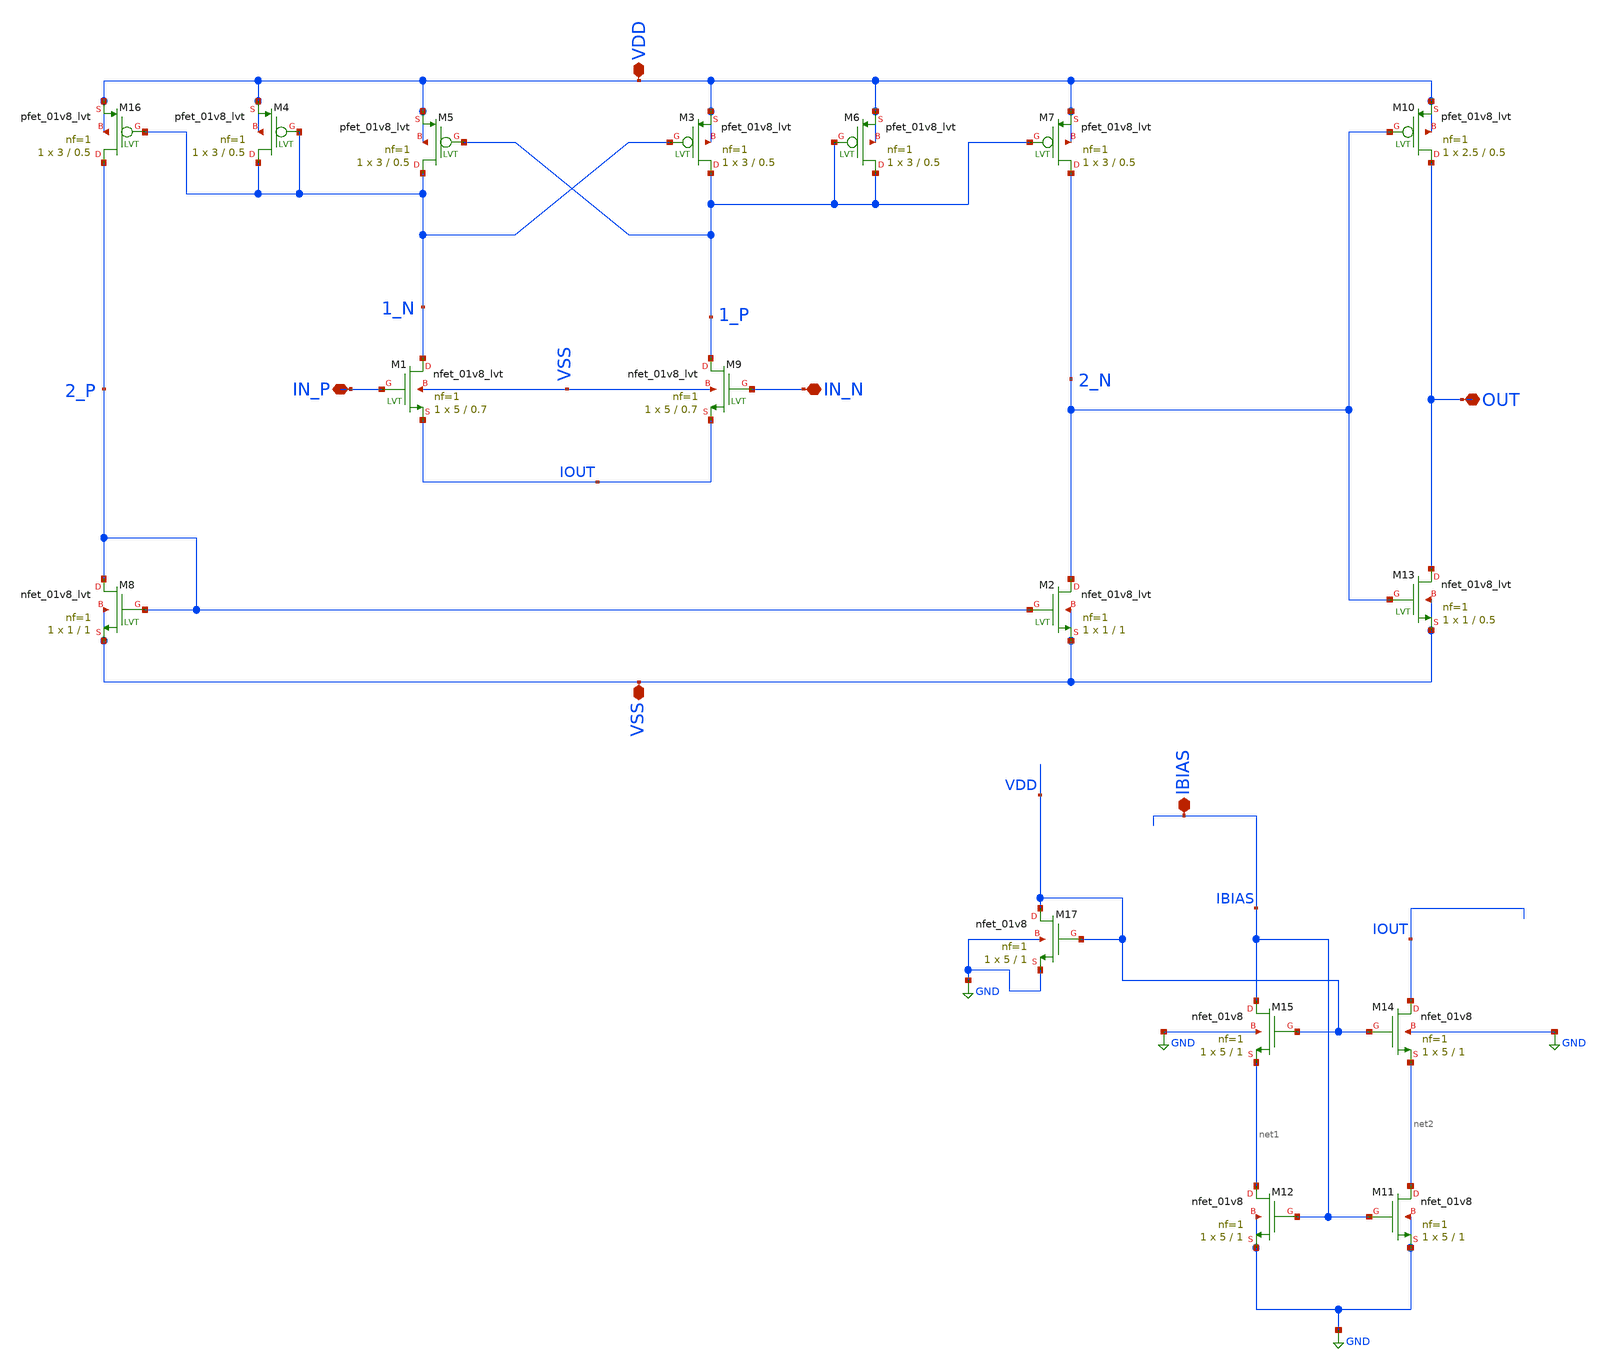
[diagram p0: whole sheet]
** sch_path: xschem/DC_DC_Converter_xschem/OTHERS/DC_DC_Converter_JV11/Comparator/comp_lvt_current_mirror.sch
**.subckt comp_lvt_current_mirror VSS VDD IN_P IN_N OUT IBIAS
*.iopin VSS
*.iopin VDD
*.iopin IN_P
*.iopin IN_N
*.iopin OUT
*.iopin IBIAS
XM16 2_P 1_N VDD VDD sky130_fd_pr__pfet_01v8_lvt L=0.5 W=3 nf=1 ad='int((nf+1)/2) * W/nf * 0.29' as='int((nf+2)/2) * W/nf * 0.29'
+ pd='2*int((nf+1)/2) * (W/nf + 0.29)' ps='2*int((nf+2)/2) * (W/nf + 0.29)' nrd='0.29 / W' nrs='0.29 / W'
+ sa=0 sb=0 sd=0 mult=1 m=1
XM4 1_N 1_N VDD VDD sky130_fd_pr__pfet_01v8_lvt L=0.5 W=3 nf=1 ad='int((nf+1)/2) * W/nf * 0.29' as='int((nf+2)/2) * W/nf * 0.29'
+ pd='2*int((nf+1)/2) * (W/nf + 0.29)' ps='2*int((nf+2)/2) * (W/nf + 0.29)' nrd='0.29 / W' nrs='0.29 / W'
+ sa=0 sb=0 sd=0 mult=1 m=1
XM5 1_N 1_P VDD VDD sky130_fd_pr__pfet_01v8_lvt L=0.5 W=3 nf=1 ad='int((nf+1)/2) * W/nf * 0.29' as='int((nf+2)/2) * W/nf * 0.29'
+ pd='2*int((nf+1)/2) * (W/nf + 0.29)' ps='2*int((nf+2)/2) * (W/nf + 0.29)' nrd='0.29 / W' nrs='0.29 / W'
+ sa=0 sb=0 sd=0 mult=1 m=1
XM3 1_P 1_N VDD VDD sky130_fd_pr__pfet_01v8_lvt L=0.5 W=3 nf=1 ad='int((nf+1)/2) * W/nf * 0.29' as='int((nf+2)/2) * W/nf * 0.29'
+ pd='2*int((nf+1)/2) * (W/nf + 0.29)' ps='2*int((nf+2)/2) * (W/nf + 0.29)' nrd='0.29 / W' nrs='0.29 / W'
+ sa=0 sb=0 sd=0 mult=1 m=1
XM6 1_P 1_P VDD VDD sky130_fd_pr__pfet_01v8_lvt L=0.5 W=3 nf=1 ad='int((nf+1)/2) * W/nf * 0.29' as='int((nf+2)/2) * W/nf * 0.29'
+ pd='2*int((nf+1)/2) * (W/nf + 0.29)' ps='2*int((nf+2)/2) * (W/nf + 0.29)' nrd='0.29 / W' nrs='0.29 / W'
+ sa=0 sb=0 sd=0 mult=1 m=1
XM7 2_N 1_P VDD VDD sky130_fd_pr__pfet_01v8_lvt L=0.5 W=3 nf=1 ad='int((nf+1)/2) * W/nf * 0.29' as='int((nf+2)/2) * W/nf * 0.29'
+ pd='2*int((nf+1)/2) * (W/nf + 0.29)' ps='2*int((nf+2)/2) * (W/nf + 0.29)' nrd='0.29 / W' nrs='0.29 / W'
+ sa=0 sb=0 sd=0 mult=1 m=1
XM8 2_P 2_P VSS VSS sky130_fd_pr__nfet_01v8_lvt L=1 W=1 nf=1 ad='int((nf+1)/2) * W/nf * 0.29' as='int((nf+2)/2) * W/nf * 0.29'
+ pd='2*int((nf+1)/2) * (W/nf + 0.29)' ps='2*int((nf+2)/2) * (W/nf + 0.29)' nrd='0.29 / W' nrs='0.29 / W'
+ sa=0 sb=0 sd=0 mult=1 m=1
XM2 2_N 2_P VSS VSS sky130_fd_pr__nfet_01v8_lvt L=1 W=1 nf=1 ad='int((nf+1)/2) * W/nf * 0.29' as='int((nf+2)/2) * W/nf * 0.29'
+ pd='2*int((nf+1)/2) * (W/nf + 0.29)' ps='2*int((nf+2)/2) * (W/nf + 0.29)' nrd='0.29 / W' nrs='0.29 / W'
+ sa=0 sb=0 sd=0 mult=1 m=1
XM9 1_P IN_N IOUT VSS sky130_fd_pr__nfet_01v8_lvt L=0.7 W=5 nf=1 ad='int((nf+1)/2) * W/nf * 0.29' as='int((nf+2)/2) * W/nf * 0.29'
+ pd='2*int((nf+1)/2) * (W/nf + 0.29)' ps='2*int((nf+2)/2) * (W/nf + 0.29)' nrd='0.29 / W' nrs='0.29 / W'
+ sa=0 sb=0 sd=0 mult=1 m=1
XM1 1_N IN_P IOUT VSS sky130_fd_pr__nfet_01v8_lvt L=0.7 W=5 nf=1 ad='int((nf+1)/2) * W/nf * 0.29' as='int((nf+2)/2) * W/nf * 0.29'
+ pd='2*int((nf+1)/2) * (W/nf + 0.29)' ps='2*int((nf+2)/2) * (W/nf + 0.29)' nrd='0.29 / W' nrs='0.29 / W'
+ sa=0 sb=0 sd=0 mult=1 m=1
XM10 OUT 2_N VDD VDD sky130_fd_pr__pfet_01v8_lvt L=0.5 W=2.5 nf=1 ad='int((nf+1)/2) * W/nf * 0.29' as='int((nf+2)/2) * W/nf * 0.29'
+ pd='2*int((nf+1)/2) * (W/nf + 0.29)' ps='2*int((nf+2)/2) * (W/nf + 0.29)' nrd='0.29 / W' nrs='0.29 / W'
+ sa=0 sb=0 sd=0 mult=1 m=1
XM13 OUT 2_N VSS VSS sky130_fd_pr__nfet_01v8_lvt L=0.5 W=1 nf=1 ad='int((nf+1)/2) * W/nf * 0.29' as='int((nf+2)/2) * W/nf * 0.29'
+ pd='2*int((nf+1)/2) * (W/nf + 0.29)' ps='2*int((nf+2)/2) * (W/nf + 0.29)' nrd='0.29 / W' nrs='0.29 / W'
+ sa=0 sb=0 sd=0 mult=1 m=1
XM11 net2 IBIAS GND GND sky130_fd_pr__nfet_01v8 L=1 W=5 nf=1 ad='int((nf+1)/2) * W/nf * 0.29' as='int((nf+2)/2) * W/nf * 0.29'
+ pd='2*int((nf+1)/2) * (W/nf + 0.29)' ps='2*int((nf+2)/2) * (W/nf + 0.29)' nrd='0.29 / W' nrs='0.29 / W'
+ sa=0 sb=0 sd=0 mult=1 m=1
XM12 net1 IBIAS GND GND sky130_fd_pr__nfet_01v8 L=1 W=5 nf=1 ad='int((nf+1)/2) * W/nf * 0.29' as='int((nf+2)/2) * W/nf * 0.29'
+ pd='2*int((nf+1)/2) * (W/nf + 0.29)' ps='2*int((nf+2)/2) * (W/nf + 0.29)' nrd='0.29 / W' nrs='0.29 / W'
+ sa=0 sb=0 sd=0 mult=1 m=1
XM14 IOUT VDD net2 GND sky130_fd_pr__nfet_01v8 L=1 W=5 nf=1 ad='int((nf+1)/2) * W/nf * 0.29' as='int((nf+2)/2) * W/nf * 0.29'
+ pd='2*int((nf+1)/2) * (W/nf + 0.29)' ps='2*int((nf+2)/2) * (W/nf + 0.29)' nrd='0.29 / W' nrs='0.29 / W'
+ sa=0 sb=0 sd=0 mult=1 m=1
XM15 IBIAS VDD net1 GND sky130_fd_pr__nfet_01v8 L=1 W=5 nf=1 ad='int((nf+1)/2) * W/nf * 0.29' as='int((nf+2)/2) * W/nf * 0.29'
+ pd='2*int((nf+1)/2) * (W/nf + 0.29)' ps='2*int((nf+2)/2) * (W/nf + 0.29)' nrd='0.29 / W' nrs='0.29 / W'
+ sa=0 sb=0 sd=0 mult=1 m=1
XM17 VDD VDD GND GND sky130_fd_pr__nfet_01v8 L=1 W=5 nf=1 ad='int((nf+1)/2) * W/nf * 0.29' as='int((nf+2)/2) * W/nf * 0.29'
+ pd='2*int((nf+1)/2) * (W/nf + 0.29)' ps='2*int((nf+2)/2) * (W/nf + 0.29)' nrd='0.29 / W' nrs='0.29 / W'
+ sa=0 sb=0 sd=0 mult=1 m=1
**.ends
.GLOBAL GND
.end
